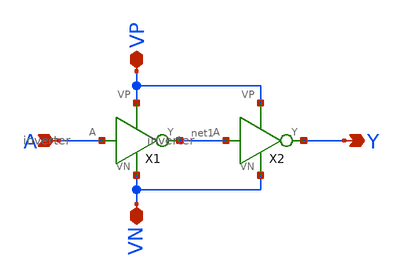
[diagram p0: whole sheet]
** sch_path: projects/inverter_tutorial/xschem_ngspice/buffer.sch
**.subckt buffer A VP VN Y
*.ipin A
*.iopin VP
*.iopin VN
*.opin Y
X1 A net1 net2 VN inverter
X2 net1 Y VP VN inverter
**.ends

* expanding   symbol:
*+  /foss/designs/my_design/projects/inverter_tutorial/xschem_ngspice/inverter.sym # of pins=4
** sym_path: projects/inverter_tutorial/xschem_ngspice/inverter.sym
** sch_path: projects/inverter_tutorial/xschem_ngspice/inverter.sch
.subckt inverter A Y VP VN
*.ipin A
*.iopin VP
*.iopin VN
*.opin Y
XM1 Y A VN VN sky130_fd_pr__nfet_01v8 L=0.15 W=1 nf=1 ad='int((nf+1)/2) * W/nf * 0.29' as='int((nf+2)/2) * W/nf * 0.29'
+ pd='2*int((nf+1)/2) * (W/nf + 0.29)' ps='2*int((nf+2)/2) * (W/nf + 0.29)' nrd='0.29 / W' nrs='0.29 / W'
+ sa=0 sb=0 sd=0 mult=1 m=1
XM2 Y A VP VP sky130_fd_pr__pfet_01v8 L=0.15 W=1 nf=1 ad='int((nf+1)/2) * W/nf * 0.29' as='int((nf+2)/2) * W/nf * 0.29'
+ pd='2*int((nf+1)/2) * (W/nf + 0.29)' ps='2*int((nf+2)/2) * (W/nf + 0.29)' nrd='0.29 / W' nrs='0.29 / W'
+ sa=0 sb=0 sd=0 mult=1 m=1
.ends

.end
